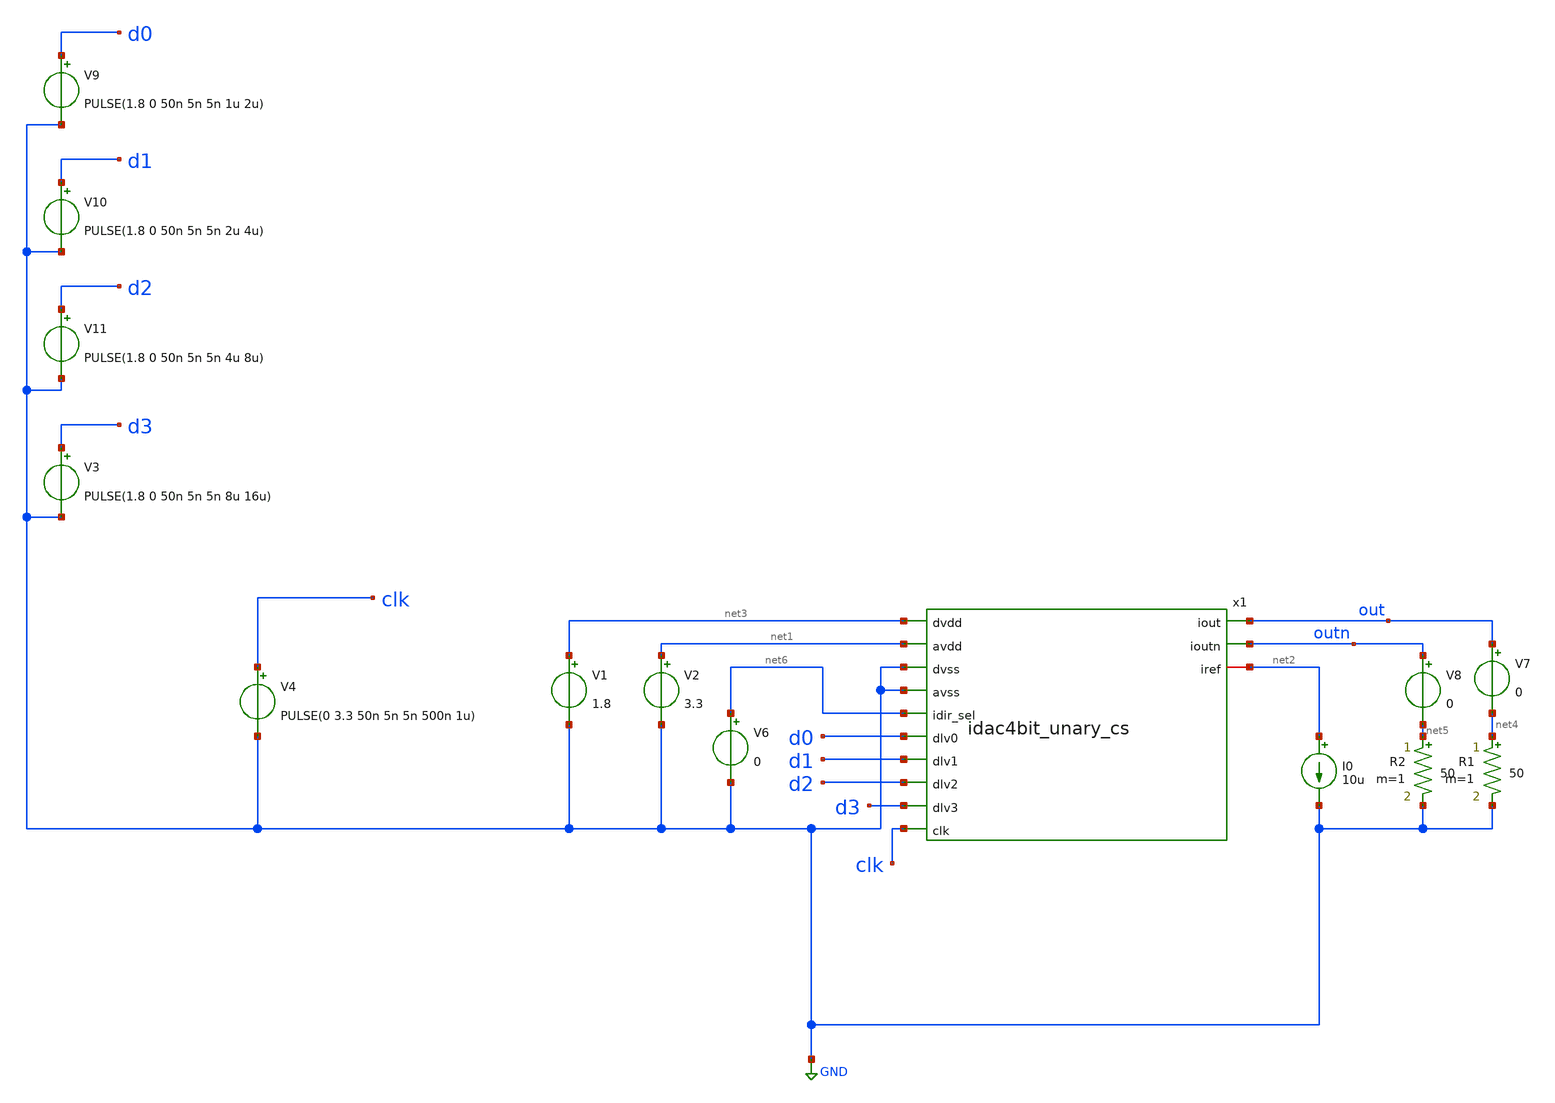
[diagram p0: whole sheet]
** sch_path: xschem/idac4bitthermo_cs_tb.sch
**.subckt idac4bitthermo_cs_tb
V1 net3 GND 1.8
V2 net1 GND 3.3
I0 net2 GND 10u
V3 d3 GND PULSE(1.8 0 50n 5n 5n 8u 16u)
V6 net6 GND 0
V7 out net4 0
R1 net4 GND 50 m=1
V8 outn net5 0
R2 net5 GND 50 m=1
V9 d0 GND PULSE(1.8 0 50n 5n 5n 1u 2u)
V10 d1 GND PULSE(1.8 0 50n 5n 5n 2u 4u)
V11 d2 GND PULSE(1.8 0 50n 5n 5n 4u 8u)
x1 net3 out net1 outn GND GND net6 d0 d1 d2 d3 clk net2 idac4bit_unary_cs
V4 clk GND PULSE(0 3.3 50n 5n 5n 500n 1u)
**** begin user architecture code
 .lib $::SKYWATER_MODELS/sky130.lib.spice tt
.include $::SKYWATER_STDCELLS/../../sky130_fd_sc_hvl/spice/sky130_fd_sc_hvl.spice

.param mc_mm_switch=0
.param mc_pr_switch=1



.option wnflag=0
.save v(out) i(V7)
.control
tran 10n 16u
plot v(out)
plot i(V7)
write currentmirrortb.raw v(out) i(V7)
.endc


**** end user architecture code
**.ends
.GLOBAL GND
.end
